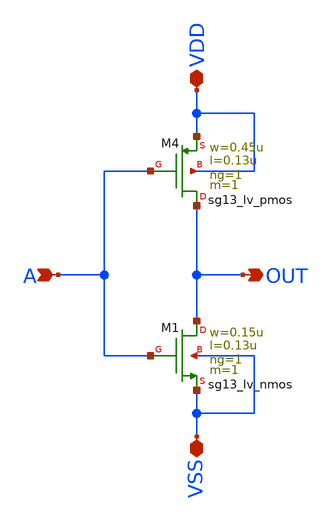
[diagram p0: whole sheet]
** sch_path: Custom_std_cells/not_custom.sch
**.subckt not_custom VDD VSS A OUT
*.iopin VDD
*.iopin VSS
*.ipin A
*.opin OUT
XM4 OUT A VDD VDD sg13_lv_pmos w=0.45u l=0.13u ng=1 m=1 mm_ok=1
XM1 OUT A VSS VSS sg13_lv_nmos w=0.15u l=0.13u ng=1 m=1 mm_ok=1
**.ends
.end
